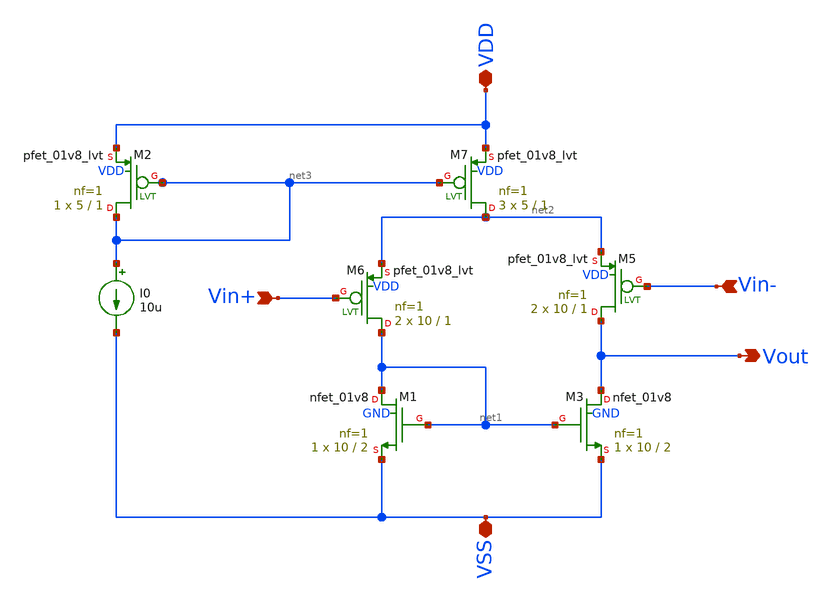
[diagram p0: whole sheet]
** sch_path: xschem/Amplifiers/5Tp.sch
**.subckt 5Tp VDD VSS Vin- Vin+ Vout
*.iopin VDD
*.iopin VSS
*.ipin Vin-
*.ipin Vin+
*.opin Vout
I0 net3 VSS 10u
XM5 Vout Vin- net2 VDD sky130_fd_pr__pfet_01v8_lvt L=1 W=10 nf=1 ad='int((nf+1)/2) * W/nf * 0.29' as='int((nf+2)/2) * W/nf * 0.29'
+ pd='2*int((nf+1)/2) * (W/nf + 0.29)' ps='2*int((nf+2)/2) * (W/nf + 0.29)' nrd='0.29 / W' nrs='0.29 / W'
+ sa=0 sb=0 sd=0 mult=2 m=2
XM6 net1 Vin+ net2 VDD sky130_fd_pr__pfet_01v8_lvt L=1 W=10 nf=1 ad='int((nf+1)/2) * W/nf * 0.29' as='int((nf+2)/2) * W/nf * 0.29'
+ pd='2*int((nf+1)/2) * (W/nf + 0.29)' ps='2*int((nf+2)/2) * (W/nf + 0.29)' nrd='0.29 / W' nrs='0.29 / W'
+ sa=0 sb=0 sd=0 mult=2 m=2
XM1 net1 net1 VSS GND sky130_fd_pr__nfet_01v8 L=2 W=10 nf=1 ad='int((nf+1)/2) * W/nf * 0.29' as='int((nf+2)/2) * W/nf * 0.29'
+ pd='2*int((nf+1)/2) * (W/nf + 0.29)' ps='2*int((nf+2)/2) * (W/nf + 0.29)' nrd='0.29 / W' nrs='0.29 / W'
+ sa=0 sb=0 sd=0 mult=1 m=1
XM3 Vout net1 VSS GND sky130_fd_pr__nfet_01v8 L=2 W=10 nf=1 ad='int((nf+1)/2) * W/nf * 0.29' as='int((nf+2)/2) * W/nf * 0.29'
+ pd='2*int((nf+1)/2) * (W/nf + 0.29)' ps='2*int((nf+2)/2) * (W/nf + 0.29)' nrd='0.29 / W' nrs='0.29 / W'
+ sa=0 sb=0 sd=0 mult=1 m=1
XM7 net2 net3 VDD VDD sky130_fd_pr__pfet_01v8_lvt L=1 W=5 nf=1 ad='int((nf+1)/2) * W/nf * 0.29' as='int((nf+2)/2) * W/nf * 0.29'
+ pd='2*int((nf+1)/2) * (W/nf + 0.29)' ps='2*int((nf+2)/2) * (W/nf + 0.29)' nrd='0.29 / W' nrs='0.29 / W'
+ sa=0 sb=0 sd=0 mult=3 m=3
XM2 net3 net3 VDD VDD sky130_fd_pr__pfet_01v8_lvt L=1 W=5 nf=1 ad='int((nf+1)/2) * W/nf * 0.29' as='int((nf+2)/2) * W/nf * 0.29'
+ pd='2*int((nf+1)/2) * (W/nf + 0.29)' ps='2*int((nf+2)/2) * (W/nf + 0.29)' nrd='0.29 / W' nrs='0.29 / W'
+ sa=0 sb=0 sd=0 mult=1 m=1
**.ends
.end
